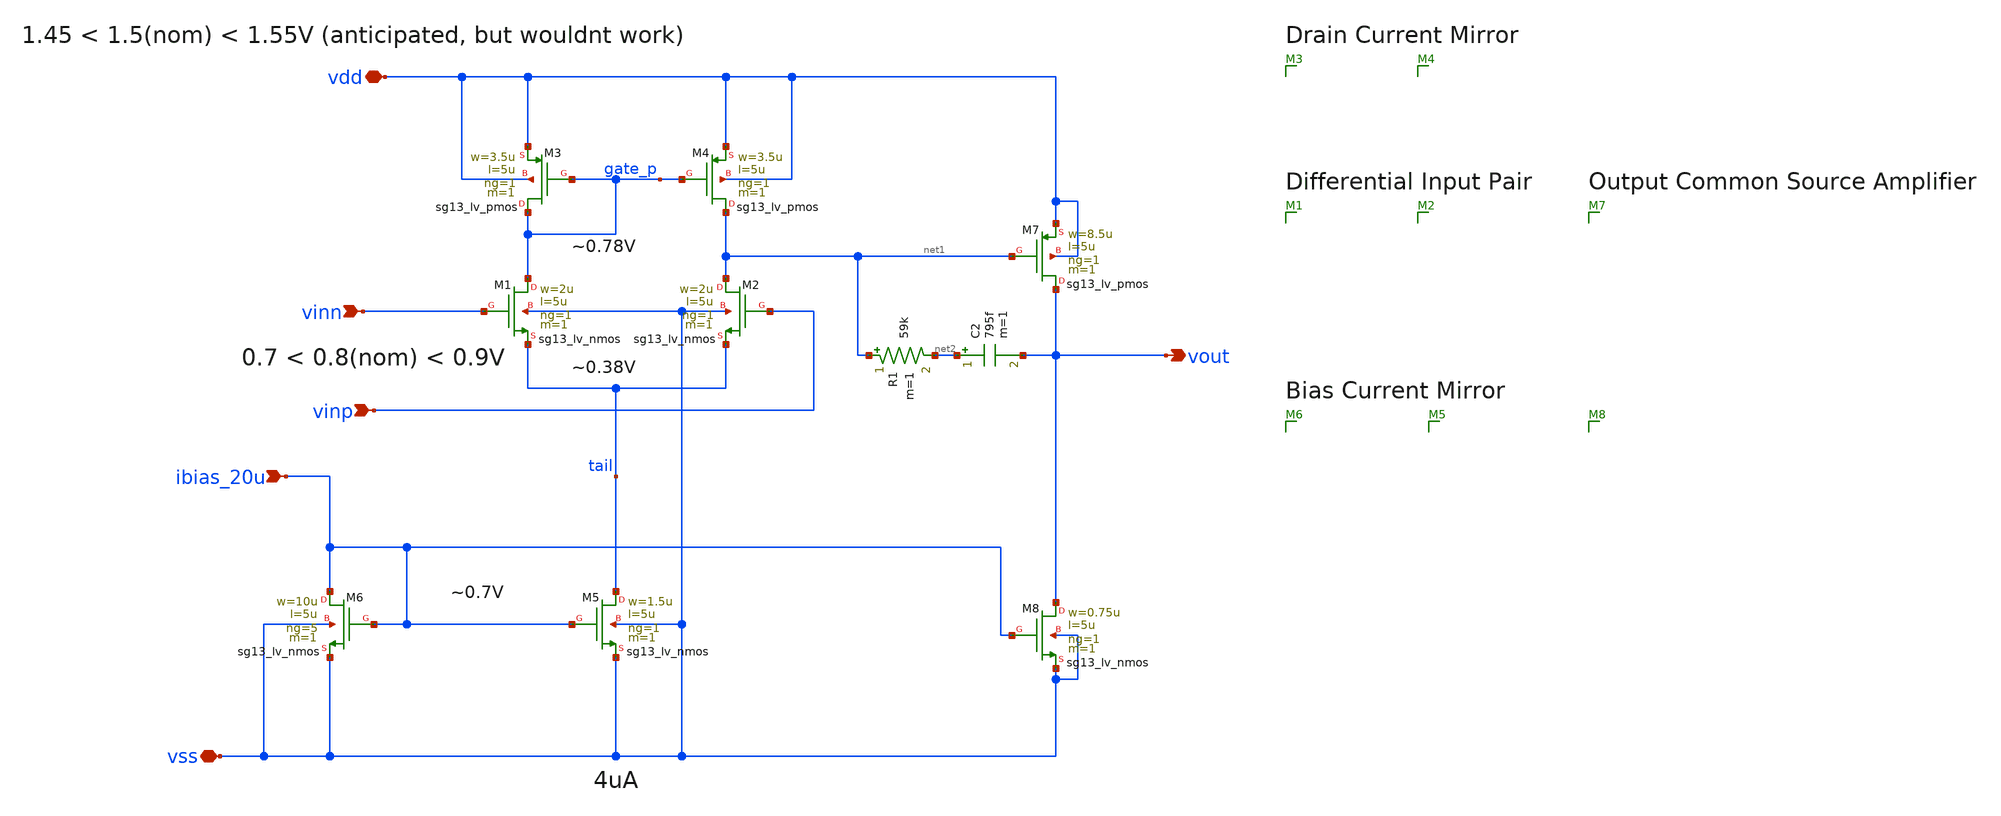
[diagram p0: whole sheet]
** sch_path: 004_Real_Circuits/003_version_second_output_stage/ota-5t_no_ena_copy.sch
**.subckt ota-5t_no_ena_copy vout vdd vinp vinn ibias_20u vss
*.opin vout
*.iopin vdd
*.ipin vinp
*.ipin vinn
*.ipin ibias_20u
*.iopin vss
XM5 tail ibias_20u vss vss sg13_lv_nmos w=1.5u l=5u ng=1 m=1 mm_ok=1
XM4 net1 gate_p vdd vdd sg13_lv_pmos w=3.5u l=5u ng=1 m=1 mm_ok=1
XM1 gate_p vinn tail vss sg13_lv_nmos w=2u l=5u ng=1 m=1 mm_ok=1
XM2 net1 vinp tail vss sg13_lv_nmos w=2u l=5u ng=1 m=1 mm_ok=1
XM3 gate_p gate_p vdd vdd sg13_lv_pmos w=3.5u l=5u ng=1 m=1 mm_ok=1
XM6 ibias_20u ibias_20u vss vss sg13_lv_nmos w=10u l=5u ng=5 m=1 mm_ok=1
XM7 vout net1 vdd vdd sg13_lv_pmos w=8.5u l=5u ng=1 m=1 mm_ok=1
XM8 vout ibias_20u vss vss sg13_lv_nmos w=0.75u l=5u ng=1 m=1 mm_ok=1
C2 net2 vout 795f m=1
R1 net1 net2 59k m=1
**.ends
.end
